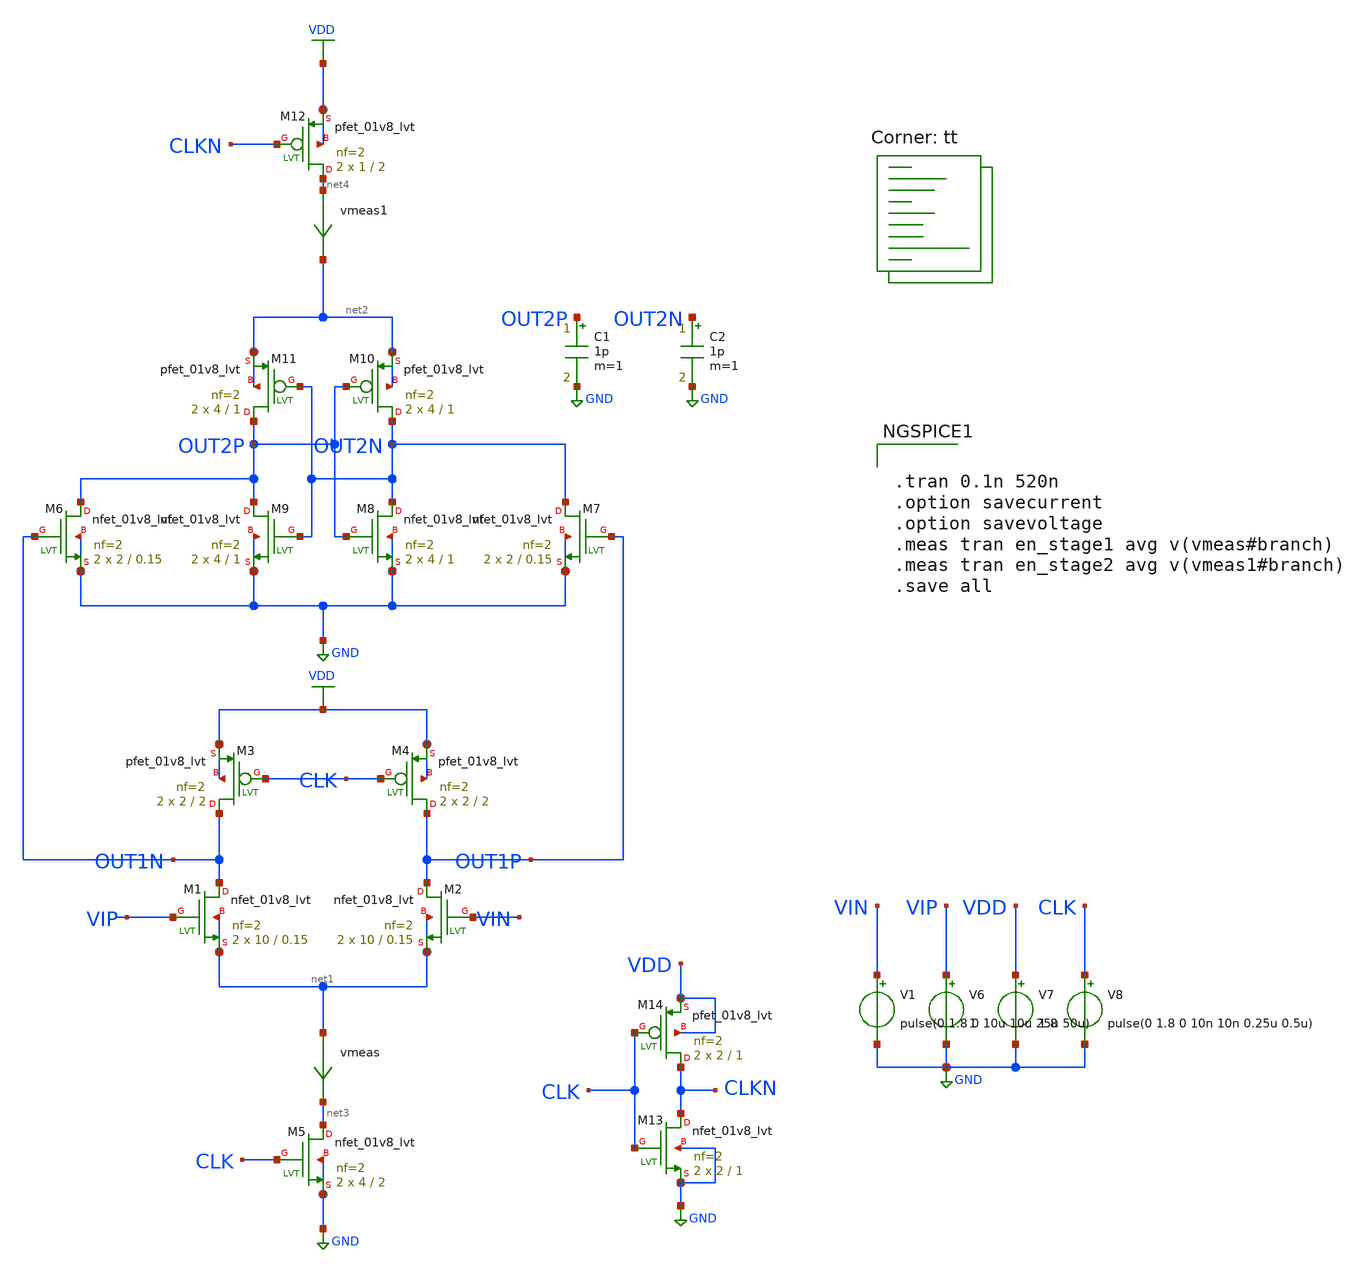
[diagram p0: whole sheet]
** sch_path: xschem/ULP_COM_POWER_COMSUMPTION.sch
**.subckt ULP_COM_POWER_COMSUMPTION
XM1 OUT1N VIP net1 net1 sky130_fd_pr__nfet_01v8_lvt L=0.15 W=10 nf=2 ad='int((nf+1)/2) * W/nf * 0.29'
+ as='int((nf+2)/2) * W/nf * 0.29' pd='2*int((nf+1)/2) * (W/nf + 0.29)' ps='2*int((nf+2)/2) * (W/nf + 0.29)'
+ nrd='0.29 / W' nrs='0.29 / W' sa=0 sb=0 sd=0 mult=2 m=2
XM2 OUT1P VIN net1 net1 sky130_fd_pr__nfet_01v8_lvt L=0.15 W=10 nf=2 ad='int((nf+1)/2) * W/nf * 0.29'
+ as='int((nf+2)/2) * W/nf * 0.29' pd='2*int((nf+1)/2) * (W/nf + 0.29)' ps='2*int((nf+2)/2) * (W/nf + 0.29)'
+ nrd='0.29 / W' nrs='0.29 / W' sa=0 sb=0 sd=0 mult=2 m=2
XM3 OUT1N CLK VDD VDD sky130_fd_pr__pfet_01v8_lvt L=2 W=2 nf=2 ad='int((nf+1)/2) * W/nf * 0.29' as='int((nf+2)/2) * W/nf * 0.29'
+ pd='2*int((nf+1)/2) * (W/nf + 0.29)' ps='2*int((nf+2)/2) * (W/nf + 0.29)' nrd='0.29 / W' nrs='0.29 / W'
+ sa=0 sb=0 sd=0 mult=2 m=2
XM4 OUT1P CLK VDD VDD sky130_fd_pr__pfet_01v8_lvt L=2 W=2 nf=2 ad='int((nf+1)/2) * W/nf * 0.29' as='int((nf+2)/2) * W/nf * 0.29'
+ pd='2*int((nf+1)/2) * (W/nf + 0.29)' ps='2*int((nf+2)/2) * (W/nf + 0.29)' nrd='0.29 / W' nrs='0.29 / W'
+ sa=0 sb=0 sd=0 mult=2 m=2
XM5 net3 CLK GND GND sky130_fd_pr__nfet_01v8_lvt L=2 W=4 nf=2 ad='int((nf+1)/2) * W/nf * 0.29' as='int((nf+2)/2) * W/nf * 0.29'
+ pd='2*int((nf+1)/2) * (W/nf + 0.29)' ps='2*int((nf+2)/2) * (W/nf + 0.29)' nrd='0.29 / W' nrs='0.29 / W'
+ sa=0 sb=0 sd=0 mult=2 m=2
XM6 OUT2P OUT1N GND GND sky130_fd_pr__nfet_01v8_lvt L=0.15 W=2 nf=2 ad='int((nf+1)/2) * W/nf * 0.29'
+ as='int((nf+2)/2) * W/nf * 0.29' pd='2*int((nf+1)/2) * (W/nf + 0.29)' ps='2*int((nf+2)/2) * (W/nf + 0.29)'
+ nrd='0.29 / W' nrs='0.29 / W' sa=0 sb=0 sd=0 mult=2 m=2
XM7 OUT2N OUT1P GND GND sky130_fd_pr__nfet_01v8_lvt L=0.15 W=2 nf=2 ad='int((nf+1)/2) * W/nf * 0.29'
+ as='int((nf+2)/2) * W/nf * 0.29' pd='2*int((nf+1)/2) * (W/nf + 0.29)' ps='2*int((nf+2)/2) * (W/nf + 0.29)'
+ nrd='0.29 / W' nrs='0.29 / W' sa=0 sb=0 sd=0 mult=2 m=2
XM8 OUT2N OUT2P GND GND sky130_fd_pr__nfet_01v8_lvt L=1 W=4 nf=2 ad='int((nf+1)/2) * W/nf * 0.29' as='int((nf+2)/2) * W/nf * 0.29'
+ pd='2*int((nf+1)/2) * (W/nf + 0.29)' ps='2*int((nf+2)/2) * (W/nf + 0.29)' nrd='0.29 / W' nrs='0.29 / W'
+ sa=0 sb=0 sd=0 mult=2 m=2
XM9 OUT2P OUT2N GND GND sky130_fd_pr__nfet_01v8_lvt L=1 W=4 nf=2 ad='int((nf+1)/2) * W/nf * 0.29' as='int((nf+2)/2) * W/nf * 0.29'
+ pd='2*int((nf+1)/2) * (W/nf + 0.29)' ps='2*int((nf+2)/2) * (W/nf + 0.29)' nrd='0.29 / W' nrs='0.29 / W'
+ sa=0 sb=0 sd=0 mult=2 m=2
XM10 OUT2N OUT2P net2 net2 sky130_fd_pr__pfet_01v8_lvt L=1 W=4 nf=2 ad='int((nf+1)/2) * W/nf * 0.29'
+ as='int((nf+2)/2) * W/nf * 0.29' pd='2*int((nf+1)/2) * (W/nf + 0.29)' ps='2*int((nf+2)/2) * (W/nf + 0.29)'
+ nrd='0.29 / W' nrs='0.29 / W' sa=0 sb=0 sd=0 mult=2 m=2
XM11 OUT2P OUT2N net2 net2 sky130_fd_pr__pfet_01v8_lvt L=1 W=4 nf=2 ad='int((nf+1)/2) * W/nf * 0.29'
+ as='int((nf+2)/2) * W/nf * 0.29' pd='2*int((nf+1)/2) * (W/nf + 0.29)' ps='2*int((nf+2)/2) * (W/nf + 0.29)'
+ nrd='0.29 / W' nrs='0.29 / W' sa=0 sb=0 sd=0 mult=2 m=2
XM12 net4 CLKN VDD VDD sky130_fd_pr__pfet_01v8_lvt L=2 W=1 nf=2 ad='int((nf+1)/2) * W/nf * 0.29' as='int((nf+2)/2) * W/nf * 0.29'
+ pd='2*int((nf+1)/2) * (W/nf + 0.29)' ps='2*int((nf+2)/2) * (W/nf + 0.29)' nrd='0.29 / W' nrs='0.29 / W'
+ sa=0 sb=0 sd=0 mult=2 m=2
vmeas net1 net3 0
.save i(vmeas)
vmeas1 net4 net2 0
.save i(vmeas1)
C1 OUT2P GND 1p m=1
C2 OUT2N GND 1p m=1
XM13 CLKN CLK GND GND sky130_fd_pr__nfet_01v8_lvt L=1 W=2 nf=2 ad='int((nf+1)/2) * W/nf * 0.29' as='int((nf+2)/2) * W/nf * 0.29'
+ pd='2*int((nf+1)/2) * (W/nf + 0.29)' ps='2*int((nf+2)/2) * (W/nf + 0.29)' nrd='0.29 / W' nrs='0.29 / W'
+ sa=0 sb=0 sd=0 mult=2 m=2
XM14 CLKN CLK VDD VDD sky130_fd_pr__pfet_01v8_lvt L=1 W=2 nf=2 ad='int((nf+1)/2) * W/nf * 0.29' as='int((nf+2)/2) * W/nf * 0.29'
+ pd='2*int((nf+1)/2) * (W/nf + 0.29)' ps='2*int((nf+2)/2) * (W/nf + 0.29)' nrd='0.29 / W' nrs='0.29 / W'
+ sa=0 sb=0 sd=0 mult=2 m=2
V6 VIP GND 1
V7 VDD GND 1.8
V8 CLK GND pulse(0 1.8 0 10n 10n 0.25u 0.5u)
V1 VIN GND pulse(0 1.8 0 10u 10u 25u 50u)
**** begin user architecture code


.tran 0.1n 520n
.option savecurrent
.option savevoltage
.meas tran en_stage1 avg v(vmeas#branch)
.meas tran en_stage2 avg v(vmeas1#branch)
.save all

.lib $::SKYWATER_MODELS/sky130.lib.spice tt
**** end user architecture code
**.ends
.GLOBAL GND
.GLOBAL VDD
.end
